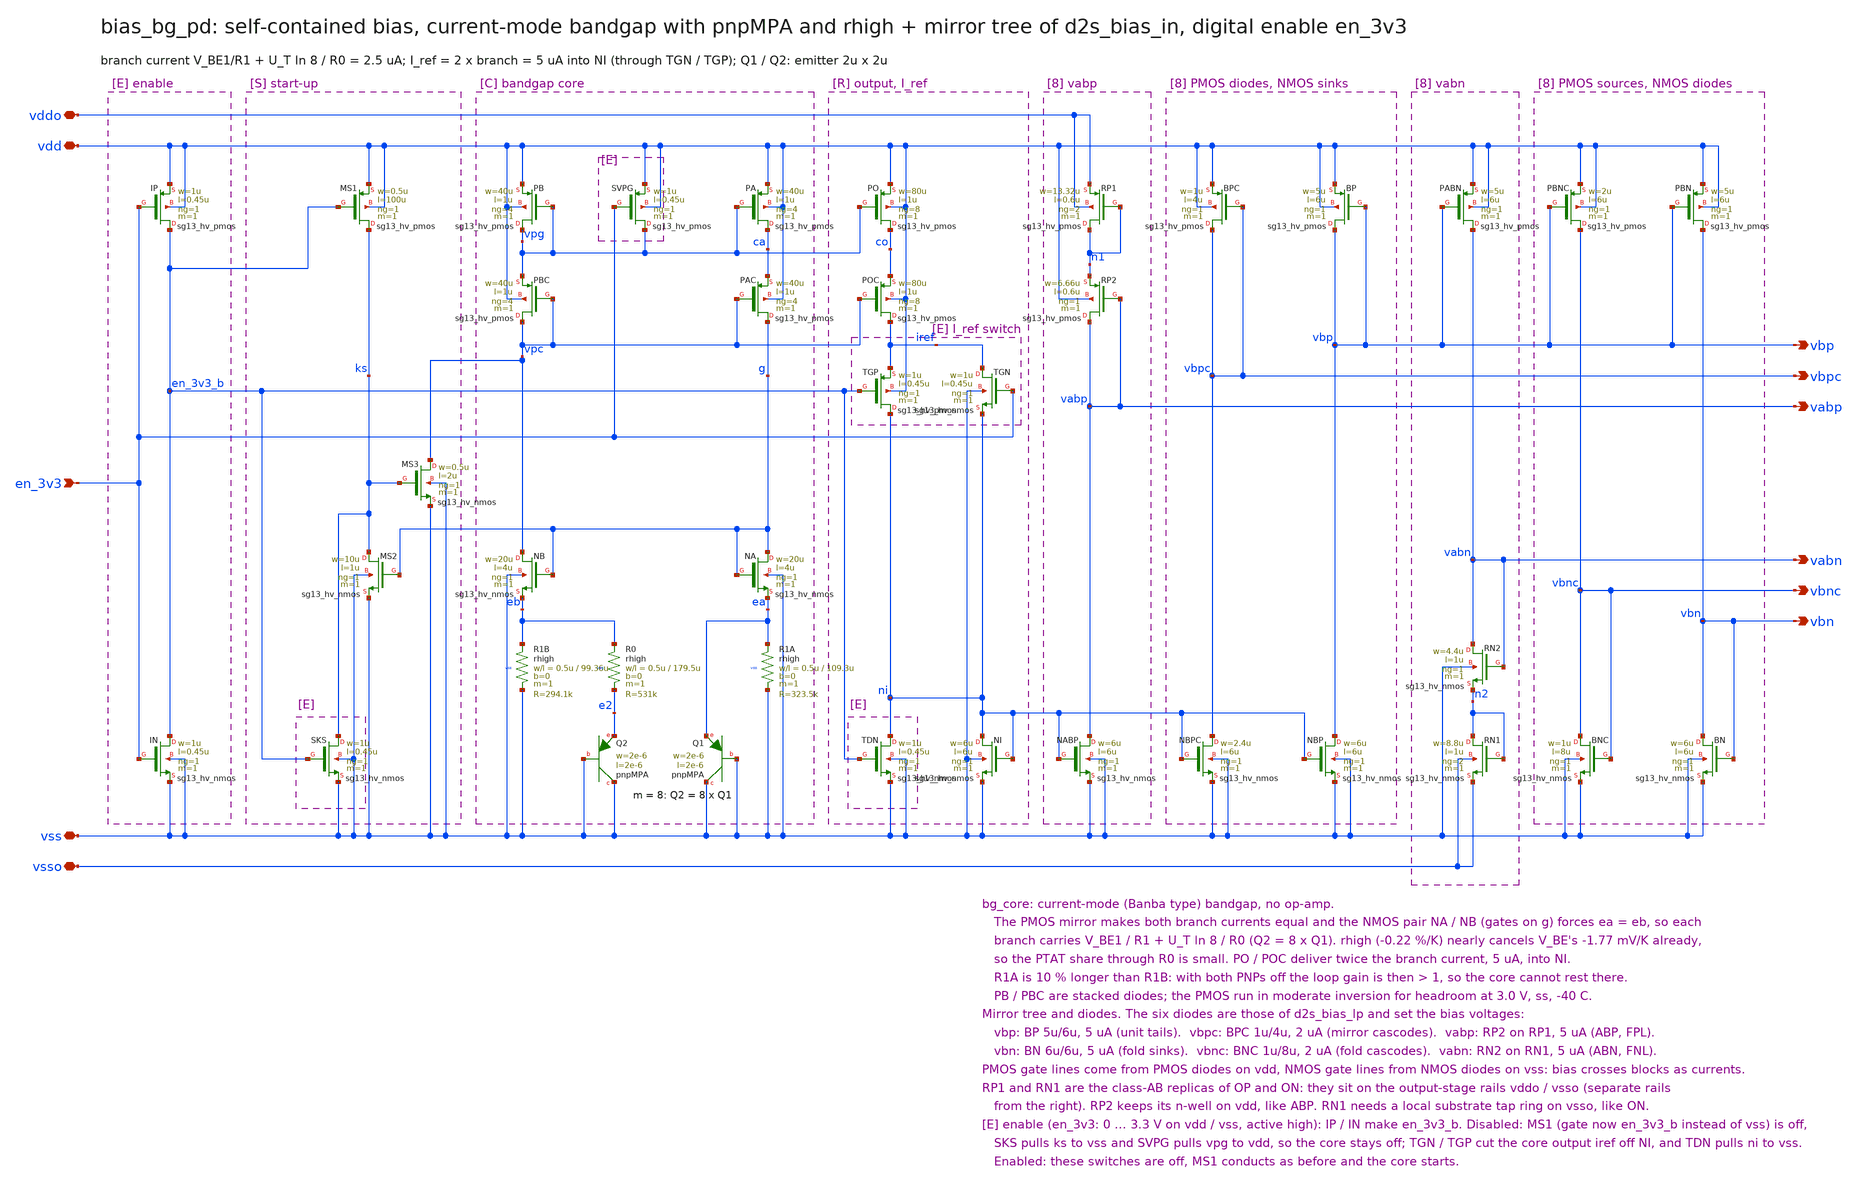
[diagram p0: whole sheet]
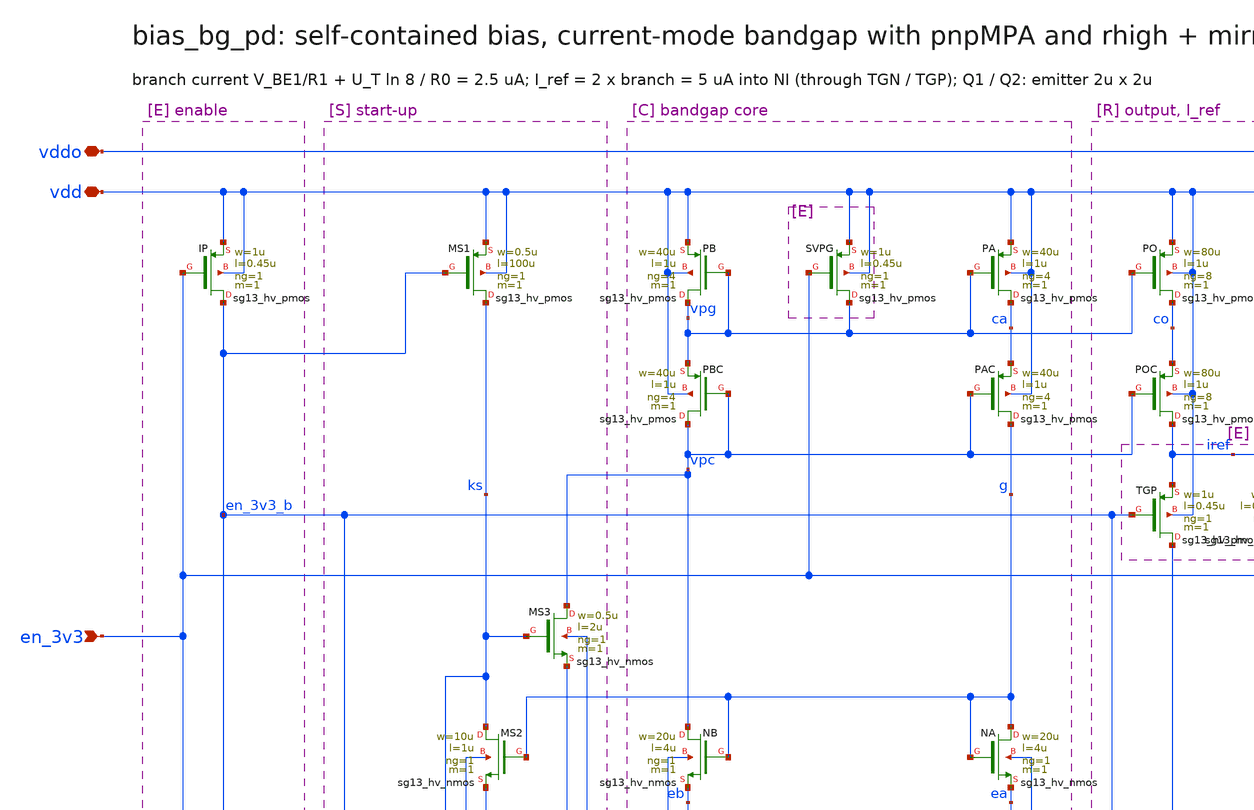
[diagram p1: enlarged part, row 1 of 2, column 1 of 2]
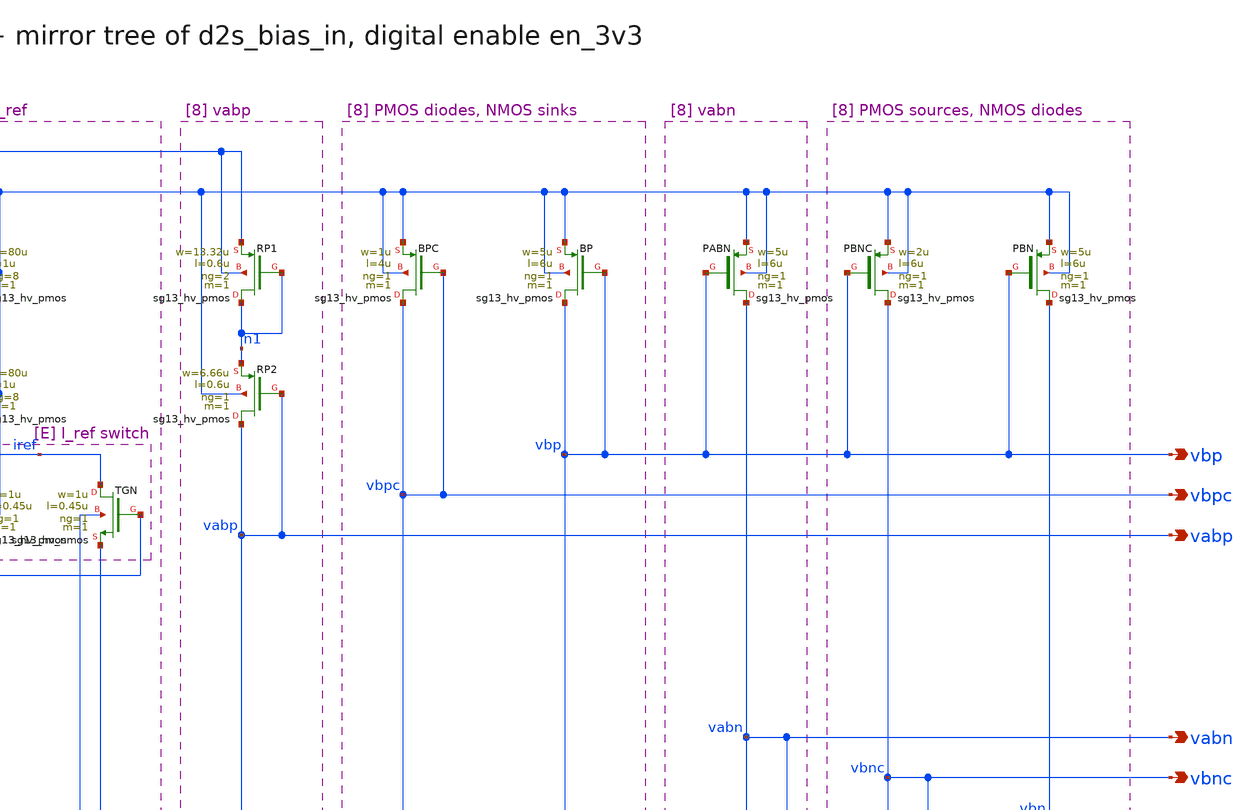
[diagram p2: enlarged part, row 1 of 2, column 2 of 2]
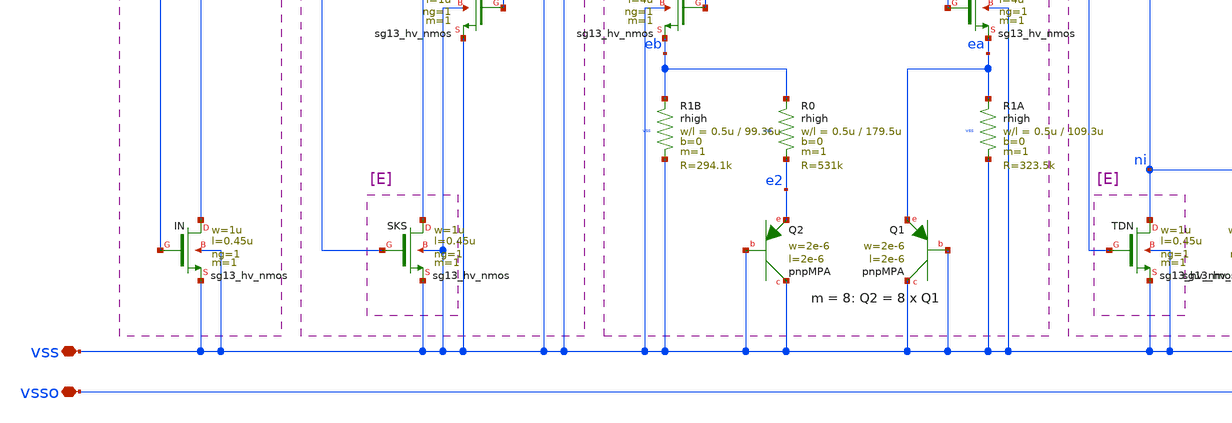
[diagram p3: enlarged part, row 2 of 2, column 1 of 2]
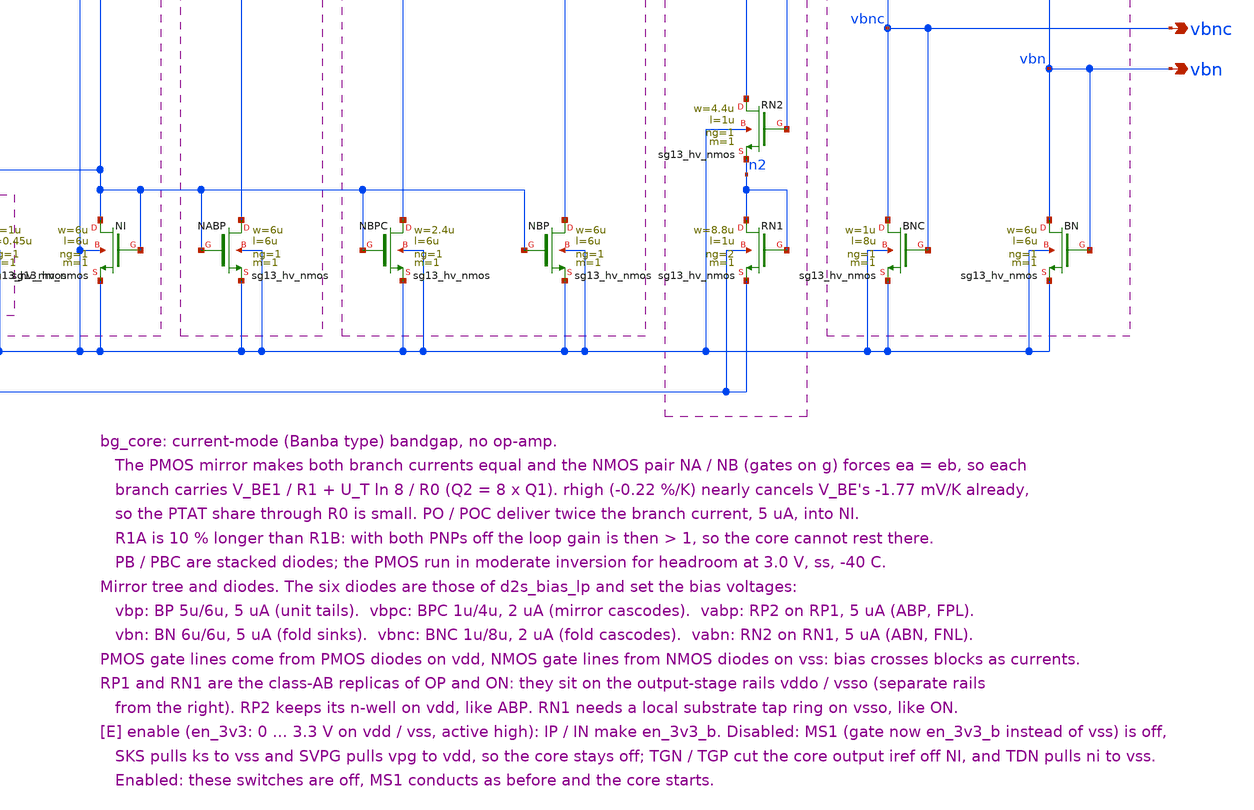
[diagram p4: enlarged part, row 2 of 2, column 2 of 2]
** sch_path: sudelbuecher/design_considerations/consolidation/ab_regroup_2026-10-28/before/macros/bias_bg_pd/schematic/xschem/bias_bg_pd.sch
**.subckt bias_bg_pd vdd vss vddo vsso vbp vbn vbpc vbnc vabp vabn en_3v3
*.iopin vdd
*.iopin vss
*.iopin vddo
*.iopin vsso
*.opin vbp
*.opin vbn
*.opin vbpc
*.opin vbnc
*.opin vabp
*.opin vabn
*.ipin en_3v3
XMS1 ks en_3v3_b vdd vdd sg13_hv_pmos w=0.5u l=100u ng=1 m=1 mm_ok=1
XMS2 ks g vss vss sg13_hv_nmos w=10u l=1u ng=1 m=1 mm_ok=1
XMS3 vpc ks vss vss sg13_hv_nmos w=0.5u l=2u ng=1 m=1 mm_ok=1
XPB vpg vpg vdd vdd sg13_hv_pmos w=40u l=1u ng=4 m=1 mm_ok=1
XPBC vpc vpc vpg vdd sg13_hv_pmos w=40u l=1u ng=4 m=1 mm_ok=1
XNB vpc g eb vss sg13_hv_nmos w=20u l=4u ng=1 m=1 mm_ok=1
XR1B eb vss vss rhigh w=0.5u l=99.36u m=1 b=0 mm_ok=1
XR0 eb e2 vss rhigh w=0.5u l=179.5u m=1 b=0 mm_ok=1
XQ2 vss vss e2 pnpMPA a=4p p=8u m=8
XPA ca vpg vdd vdd sg13_hv_pmos w=40u l=1u ng=4 m=1 mm_ok=1
XPAC g vpc ca vdd sg13_hv_pmos w=40u l=1u ng=4 m=1 mm_ok=1
XNA g g ea vss sg13_hv_nmos w=20u l=4u ng=1 m=1 mm_ok=1
XR1A ea vss vss rhigh w=0.5u l=109.3u m=1 b=0 mm_ok=1
XQ1 vss vss ea pnpMPA a=4p p=8u m=1
XPO co vpg vdd vdd sg13_hv_pmos w=80u l=1u ng=8 m=1 mm_ok=1
XPOC iref vpc co vdd sg13_hv_pmos w=80u l=1u ng=8 m=1 mm_ok=1
XNI ni ni vss vss sg13_hv_nmos w=6u l=6u ng=1 m=1 mm_ok=1
XBPC vbpc vbpc vdd vdd sg13_hv_pmos w=1u l=4u ng=1 m=1 mm_ok=1
XNBPC vbpc ni vss vss sg13_hv_nmos w=2.4u l=6u ng=1 m=1 mm_ok=1
XBP vbp vbp vdd vdd sg13_hv_pmos w=5u l=6u ng=1 m=1 mm_ok=1
XNBP vbp ni vss vss sg13_hv_nmos w=6u l=6u ng=1 m=1 mm_ok=1
XRP1 n1 n1 vddo vddo sg13_hv_pmos w=13.32u l=0.6u ng=2 m=1 mm_ok=1
XRP2 vabp vabp n1 vdd sg13_hv_pmos w=6.66u l=0.6u ng=1 m=1 mm_ok=1
XNABP vabp ni vss vss sg13_hv_nmos w=6u l=6u ng=1 m=1 mm_ok=1
XPBNC vbnc vbp vdd vdd sg13_hv_pmos w=2u l=6u ng=1 m=1 mm_ok=1
XBNC vbnc vbnc vss vss sg13_hv_nmos w=1u l=8u ng=1 m=1 mm_ok=1
XPBN vbn vbp vdd vdd sg13_hv_pmos w=5u l=6u ng=1 m=1 mm_ok=1
XBN vbn vbn vss vss sg13_hv_nmos w=6u l=6u ng=1 m=1 mm_ok=1
XPABN vabn vbp vdd vdd sg13_hv_pmos w=5u l=6u ng=1 m=1 mm_ok=1
XRN2 vabn vabn n2 vss sg13_hv_nmos w=4.4u l=1u ng=1 m=1 mm_ok=1
XRN1 n2 n2 vsso vsso sg13_hv_nmos w=8.8u l=1u ng=2 m=1 mm_ok=1
XIP en_3v3_b en_3v3 vdd vdd sg13_hv_pmos w=1u l=0.45u ng=1 m=1 mm_ok=1
XIN en_3v3_b en_3v3 vss vss sg13_hv_nmos w=1u l=0.45u ng=1 m=1 mm_ok=1
XSKS ks en_3v3_b vss vss sg13_hv_nmos w=1u l=0.45u ng=1 m=1 mm_ok=1
XSVPG vpg en_3v3 vdd vdd sg13_hv_pmos w=1u l=0.45u ng=1 m=1 mm_ok=1
XTGP ni en_3v3_b iref vdd sg13_hv_pmos w=1u l=0.45u ng=1 m=1 mm_ok=1
XTGN iref en_3v3 ni vss sg13_hv_nmos w=1u l=0.45u ng=1 m=1 mm_ok=1
XTDN ni en_3v3_b vss vss sg13_hv_nmos w=1u l=0.45u ng=1 m=1 mm_ok=1
**.ends
.end
